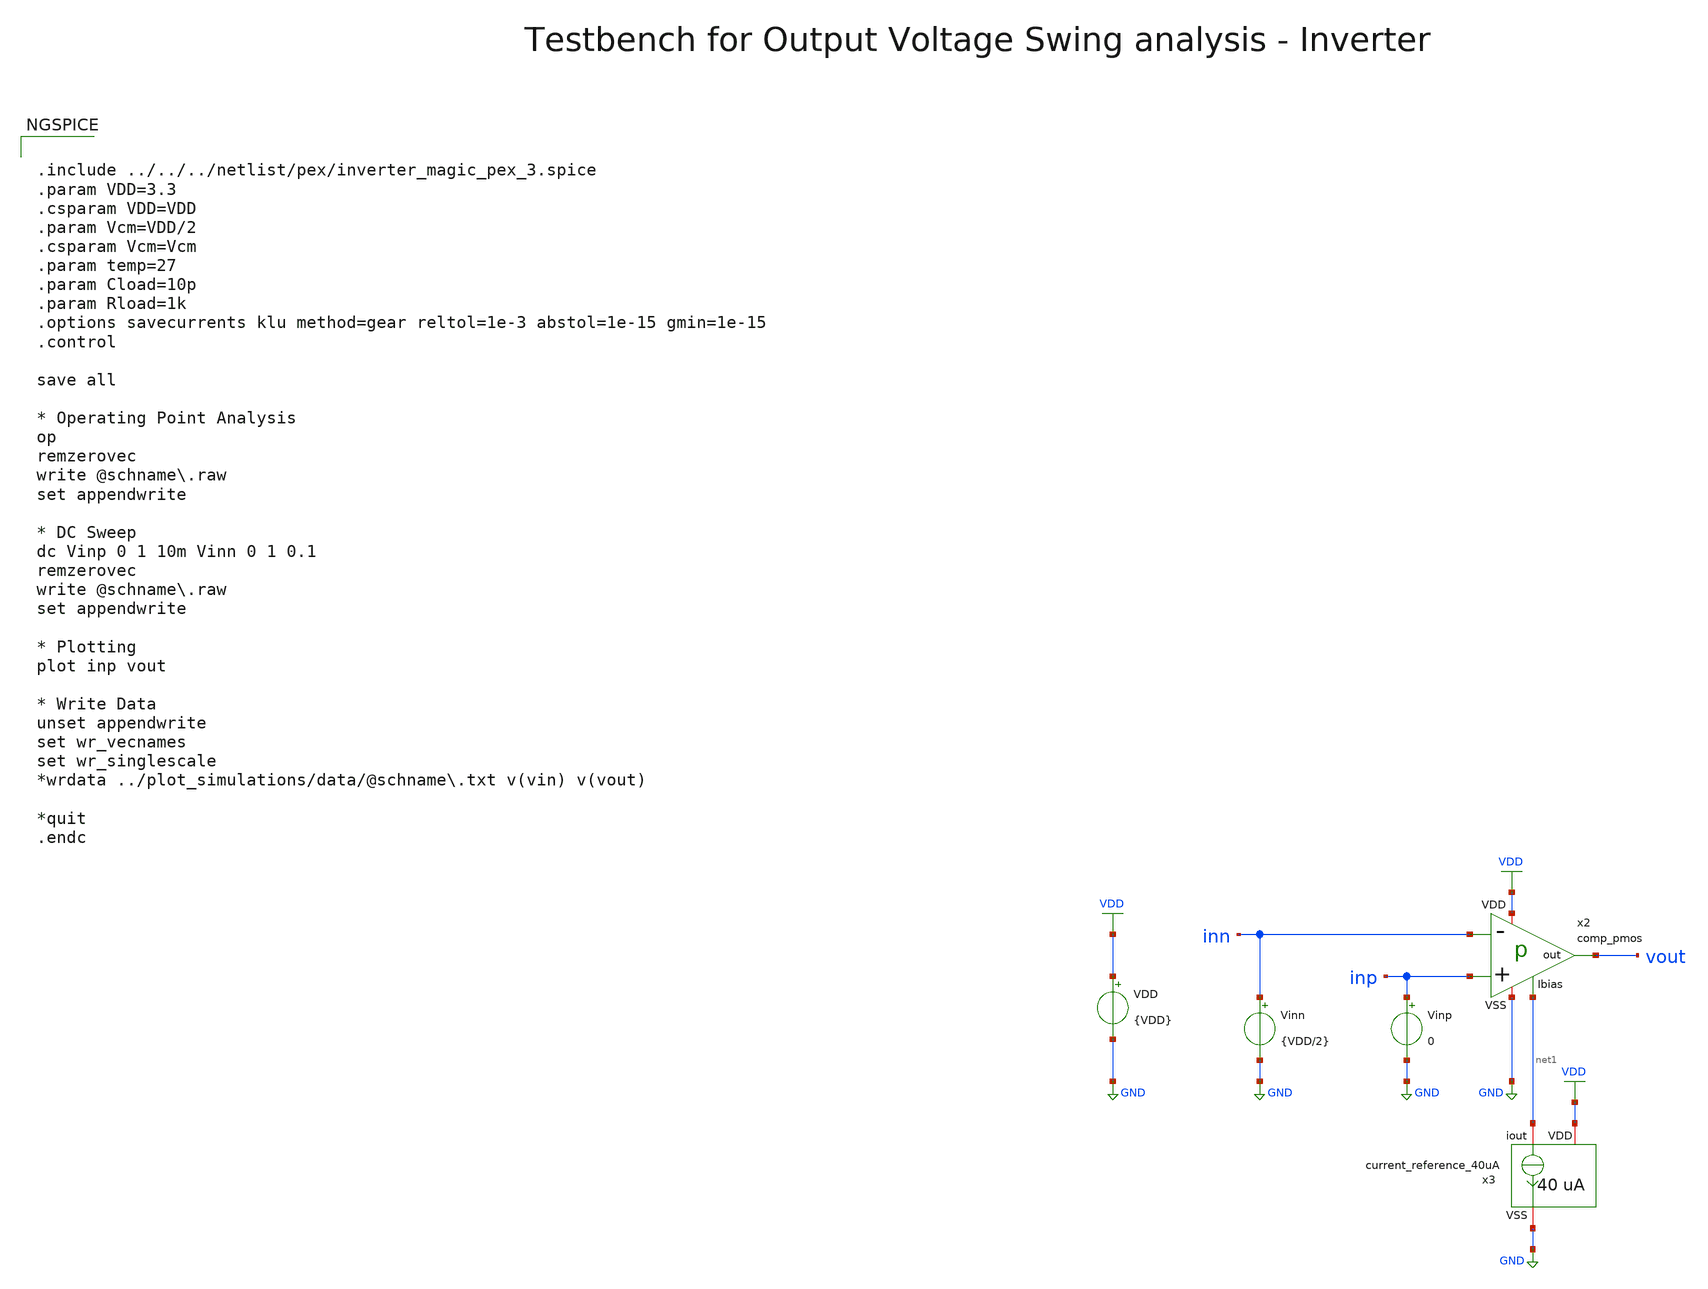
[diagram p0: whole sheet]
** sch_path: macros/heichips26_vcr/macros/switched_capacitor/testbenches/xschem/tb_comp_pmos_dc.sch
**.subckt tb_comp_pmos_dc
VDD VDD GND {VDD}
Vinp inp GND 0
Vinn inn GND {VDD/2}
x2 vout inn inp VDD net1 GND comp_pmos
x3 VDD net1 GND current_reference_40uA
**** begin user architecture code


.include ../../../netlist/pex/inverter_magic_pex_3.spice
.param VDD=3.3
.csparam VDD=VDD
.param Vcm=VDD/2
.csparam Vcm=Vcm
.param temp=27
.param Cload=10p
.param Rload=1k
.options savecurrents klu method=gear reltol=1e-3 abstol=1e-15 gmin=1e-15
.control

save all

* Operating Point Analysis
op
remzerovec
write @schname\.raw
set appendwrite

* DC Sweep
dc Vinp 0 1 10m Vinn 0 1 0.1
remzerovec
write @schname\.raw
set appendwrite

* Plotting
plot inp vout

* Write Data
unset appendwrite
set wr_vecnames
set wr_singlescale
*wrdata ../plot_simulations/data/@schname\.txt v(vin) v(vout)

*quit
.endc



.lib cornerMOSlv.lib mos_tt
.lib cornerMOShv.lib mos_tt
.lib cornerRES.lib res_typ
.lib cornerDIO.lib dio_tt

**** end user architecture code
**.ends

* expanding   symbol:  comp_pmos.sym # of pins=6
** sym_path: macros/heichips26_vcr/macros/switched_capacitor/schematic/xschem/comp_pmos.sym
** sch_path: macros/heichips26_vcr/macros/switched_capacitor/schematic/xschem/comp_pmos.sch
.subckt comp_pmos out - + VDD Ibias VSS
*.iopin VDD
*.iopin VSS
*.ipin Ibias
*.opin out
*.ipin +
*.ipin -
**** begin user architecture code


.param n_w = 1.2u
.param n_l = 1.5u
.param p_w = 2u
.param p_l = 0.4u
.param bcm = 1


**** end user architecture code
XM9 net1 Ibias VDD VDD sg13_hv_pmos w=bcm*p_w l=p_l ng=1 m=1 mm_ok=1
XM10 out Ibias VDD VDD sg13_hv_pmos w=bcm*p_w l=p_l ng=1 m=1 mm_ok=1
XM11 Ibias Ibias VDD VDD sg13_hv_pmos w=p_w l=p_l ng=1 m=1 mm_ok=1
XM12 net3 + net1 VDD sg13_hv_pmos w=p_w l=p_l ng=1 m=1 mm_ok=1
XM13 net2 - net1 VDD sg13_hv_pmos w=p_w l=p_l ng=1 m=1 mm_ok=1
XM14 net3 net2 VSS VSS sg13_hv_nmos w=n_w l=n_l ng=1 m=1 mm_ok=1
XM15 net2 net2 VSS VSS sg13_hv_nmos w=n_w l=n_l ng=1 m=1 mm_ok=1
XM16 out net3 VSS VSS sg13_hv_nmos w=n_w l=n_l ng=1 m=1 mm_ok=1
.ends


* expanding   symbol:  current_reference_40uA.sym # of pins=3
** sym_path: macros/heichips26_vcr/macros/switched_capacitor/schematic/xschem/current_reference_40uA.sym
** sch_path: macros/heichips26_vcr/macros/switched_capacitor/schematic/xschem/current_reference_40uA.sch
.subckt current_reference_40uA VDD iout VSS
*.iopin VSS
*.iopin VDD
*.iopin iout
XM8 net2 net2 VSS VSS sg13_hv_nmos w=n_w l=n_l ng=1 m=1 mm_ok=1
XM6 net2 net1 VDD VDD sg13_hv_pmos w=p_w l=p_l ng=1 m=1 mm_ok=1
XM1 net1 net1 VDD VDD sg13_hv_pmos w=p_w l=p_l ng=1 m=1 mm_ok=1
XM3 net1 net2 net3 VSS sg13_hv_nmos w=n_w l=n_l ng=1 m=1 mm_ok=1
XR2 net4 VSS VSS rppd w=2e-6 l=21.9e-6 m=1 b=0 mm_ok=1
XM2 net1 net2 net3 VSS sg13_hv_nmos w=n_w l=n_l ng=1 m=1 mm_ok=1
XM4 net1 net2 net3 VSS sg13_hv_nmos w=n_w l=n_l ng=1 m=1 mm_ok=1
XM5 net1 net2 net3 VSS sg13_hv_nmos w=n_w l=n_l ng=1 m=1 mm_ok=1
XM7 iout net2 VSS VSS sg13_hv_nmos w=n_w l=n_l ng=1 m=1 mm_ok=1
XR3 net3 net4 VSS rsil w=0.5e-6 l=365e-6 m=1 mm_ok=1
**** begin user architecture code


.param n_w = 6u
.param n_l = 5u
.param p_w = 10u
.param p_l = 2u


**** end user architecture code
.ends

.GLOBAL GND
.GLOBAL VDD
.end
